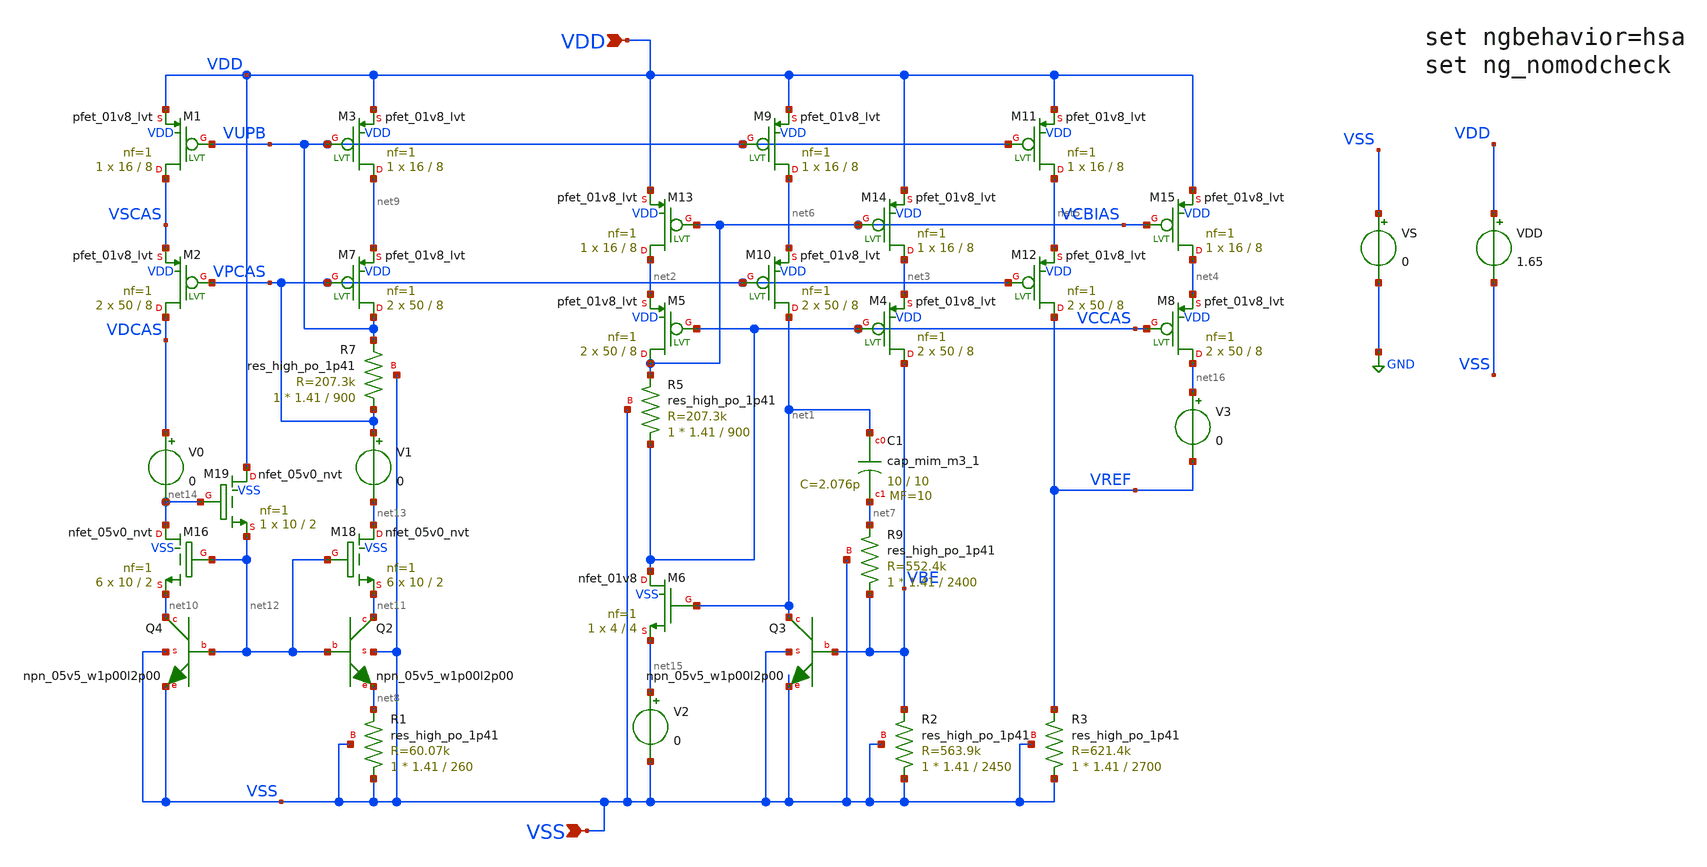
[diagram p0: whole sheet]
** sch_path: testbenches/parallel_bandgap_dc_sweep.sch
**.subckt parallel_bandgap_dc_sweep VDD VSS
*.ipin VDD
*.ipin VSS
VDD VDD VSS 1.65
.save i(vdd)
VS VSS GND 0
XQ3 net1 VBE VSS VSS sky130_fd_pr__npn_05v5_w1p00l2p00
XR2 VSS VBE VSS sky130_fd_pr__res_high_po_1p41 L=2450 mult=1 m=1
XM4 VBE VCCAS net3 VDD sky130_fd_pr__pfet_01v8_lvt L=8 W=50 nf=1 ad='int((nf+1)/2) * W/nf * 0.29' as='int((nf+2)/2) * W/nf * 0.29'
+ pd='2*int((nf+1)/2) * (W/nf + 0.29)' ps='2*int((nf+2)/2) * (W/nf + 0.29)' nrd='0.29 / W' nrs='0.29 / W'
+ sa=0 sb=0 sd=0 mult=2 m=2
XM5 VCBIAS VCCAS net2 VDD sky130_fd_pr__pfet_01v8_lvt L=8 W=50 nf=1 ad='int((nf+1)/2) * W/nf * 0.29'
+ as='int((nf+2)/2) * W/nf * 0.29' pd='2*int((nf+1)/2) * (W/nf + 0.29)' ps='2*int((nf+2)/2) * (W/nf + 0.29)'
+ nrd='0.29 / W' nrs='0.29 / W' sa=0 sb=0 sd=0 mult=2 m=2
XM6 VCCAS net1 net15 VSS sky130_fd_pr__nfet_01v8 L=4 W=4 nf=1 ad='int((nf+1)/2) * W/nf * 0.29' as='int((nf+2)/2) * W/nf * 0.29'
+ pd='2*int((nf+1)/2) * (W/nf + 0.29)' ps='2*int((nf+2)/2) * (W/nf + 0.29)' nrd='0.29 / W' nrs='0.29 / W'
+ sa=0 sb=0 sd=0 mult=1 m=1
XR3 VSS VREF VSS sky130_fd_pr__res_high_po_1p41 L=2700 mult=1 m=1
XM8 net16 VCCAS net4 VDD sky130_fd_pr__pfet_01v8_lvt L=8 W=50 nf=1 ad='int((nf+1)/2) * W/nf * 0.29' as='int((nf+2)/2) * W/nf * 0.29'
+ pd='2*int((nf+1)/2) * (W/nf + 0.29)' ps='2*int((nf+2)/2) * (W/nf + 0.29)' nrd='0.29 / W' nrs='0.29 / W'
+ sa=0 sb=0 sd=0 mult=2 m=2
XM9 net6 VUPB VDD VDD sky130_fd_pr__pfet_01v8_lvt L=8 W=16 nf=1 ad='int((nf+1)/2) * W/nf * 0.29' as='int((nf+2)/2) * W/nf * 0.29'
+ pd='2*int((nf+1)/2) * (W/nf + 0.29)' ps='2*int((nf+2)/2) * (W/nf + 0.29)' nrd='0.29 / W' nrs='0.29 / W'
+ sa=0 sb=0 sd=0 mult=1 m=1
XM10 net1 VPCAS net6 VDD sky130_fd_pr__pfet_01v8_lvt L=8 W=50 nf=1 ad='int((nf+1)/2) * W/nf * 0.29' as='int((nf+2)/2) * W/nf * 0.29'
+ pd='2*int((nf+1)/2) * (W/nf + 0.29)' ps='2*int((nf+2)/2) * (W/nf + 0.29)' nrd='0.29 / W' nrs='0.29 / W'
+ sa=0 sb=0 sd=0 mult=2 m=2
XM11 net5 VUPB VDD VDD sky130_fd_pr__pfet_01v8_lvt L=8 W=16 nf=1 ad='int((nf+1)/2) * W/nf * 0.29' as='int((nf+2)/2) * W/nf * 0.29'
+ pd='2*int((nf+1)/2) * (W/nf + 0.29)' ps='2*int((nf+2)/2) * (W/nf + 0.29)' nrd='0.29 / W' nrs='0.29 / W'
+ sa=0 sb=0 sd=0 mult=1 m=1
XM12 VREF VPCAS net5 VDD sky130_fd_pr__pfet_01v8_lvt L=8 W=50 nf=1 ad='int((nf+1)/2) * W/nf * 0.29' as='int((nf+2)/2) * W/nf * 0.29'
+ pd='2*int((nf+1)/2) * (W/nf + 0.29)' ps='2*int((nf+2)/2) * (W/nf + 0.29)' nrd='0.29 / W' nrs='0.29 / W'
+ sa=0 sb=0 sd=0 mult=2 m=2
XM13 net2 VCBIAS VDD VDD sky130_fd_pr__pfet_01v8_lvt L=8 W=16 nf=1 ad='int((nf+1)/2) * W/nf * 0.29' as='int((nf+2)/2) * W/nf * 0.29'
+ pd='2*int((nf+1)/2) * (W/nf + 0.29)' ps='2*int((nf+2)/2) * (W/nf + 0.29)' nrd='0.29 / W' nrs='0.29 / W'
+ sa=0 sb=0 sd=0 mult=1 m=1
XM14 net3 VCBIAS VDD VDD sky130_fd_pr__pfet_01v8_lvt L=8 W=16 nf=1 ad='int((nf+1)/2) * W/nf * 0.29' as='int((nf+2)/2) * W/nf * 0.29'
+ pd='2*int((nf+1)/2) * (W/nf + 0.29)' ps='2*int((nf+2)/2) * (W/nf + 0.29)' nrd='0.29 / W' nrs='0.29 / W'
+ sa=0 sb=0 sd=0 mult=1 m=1
XR5 VCCAS VCBIAS VSS sky130_fd_pr__res_high_po_1p41 L=900 mult=1 m=1
XM15 net4 VCBIAS VDD VDD sky130_fd_pr__pfet_01v8_lvt L=8 W=16 nf=1 ad='int((nf+1)/2) * W/nf * 0.29' as='int((nf+2)/2) * W/nf * 0.29'
+ pd='2*int((nf+1)/2) * (W/nf + 0.29)' ps='2*int((nf+2)/2) * (W/nf + 0.29)' nrd='0.29 / W' nrs='0.29 / W'
+ sa=0 sb=0 sd=0 mult=1 m=1
XR9 VBE net7 VSS sky130_fd_pr__res_high_po_1p41 L=2400 mult=1 m=1
XC1 net1 net7 sky130_fd_pr__cap_mim_m3_1 W=10 L=10 MF=10 m=10
V0 VDCAS net14 0
.save i(v0)
V1 VPCAS net13 0
.save i(v1)
XM3 net9 VUPB VDD VDD sky130_fd_pr__pfet_01v8_lvt L=8 W=16 nf=1 ad='int((nf+1)/2) * W/nf * 0.29' as='int((nf+2)/2) * W/nf * 0.29'
+ pd='2*int((nf+1)/2) * (W/nf + 0.29)' ps='2*int((nf+2)/2) * (W/nf + 0.29)' nrd='0.29 / W' nrs='0.29 / W'
+ sa=0 sb=0 sd=0 mult=1 m=1
XM1 VSCAS VUPB VDD VDD sky130_fd_pr__pfet_01v8_lvt L=8 W=16 nf=1 ad='int((nf+1)/2) * W/nf * 0.29' as='int((nf+2)/2) * W/nf * 0.29'
+ pd='2*int((nf+1)/2) * (W/nf + 0.29)' ps='2*int((nf+2)/2) * (W/nf + 0.29)' nrd='0.29 / W' nrs='0.29 / W'
+ sa=0 sb=0 sd=0 mult=1 m=1
XQ2 net11 net12 net8 VSS sky130_fd_pr__npn_05v5_w1p00l2p00
XQ4 net10 net12 VSS VSS sky130_fd_pr__npn_05v5_w1p00l2p00
XR1 VSS net8 VSS sky130_fd_pr__res_high_po_1p41 L=260 mult=1 m=1
XM7 VUPB VPCAS net9 VDD sky130_fd_pr__pfet_01v8_lvt L=8 W=50 nf=1 ad='int((nf+1)/2) * W/nf * 0.29' as='int((nf+2)/2) * W/nf * 0.29'
+ pd='2*int((nf+1)/2) * (W/nf + 0.29)' ps='2*int((nf+2)/2) * (W/nf + 0.29)' nrd='0.29 / W' nrs='0.29 / W'
+ sa=0 sb=0 sd=0 mult=2 m=2
XM2 VDCAS VPCAS VSCAS VDD sky130_fd_pr__pfet_01v8_lvt L=8 W=50 nf=1 ad='int((nf+1)/2) * W/nf * 0.29'
+ as='int((nf+2)/2) * W/nf * 0.29' pd='2*int((nf+1)/2) * (W/nf + 0.29)' ps='2*int((nf+2)/2) * (W/nf + 0.29)'
+ nrd='0.29 / W' nrs='0.29 / W' sa=0 sb=0 sd=0 mult=2 m=2
XR7 VPCAS VUPB VSS sky130_fd_pr__res_high_po_1p41 L=900 mult=1 m=1
XM16 net14 net12 net10 VSS sky130_fd_pr__nfet_05v0_nvt L=2 W=10 nf=1 ad='int((nf+1)/2) * W/nf * 0.29'
+ as='int((nf+2)/2) * W/nf * 0.29' pd='2*int((nf+1)/2) * (W/nf + 0.29)' ps='2*int((nf+2)/2) * (W/nf + 0.29)'
+ nrd='0.29 / W' nrs='0.29 / W' sa=0 sb=0 sd=0 mult=6 m=6
XM18 net13 net12 net11 VSS sky130_fd_pr__nfet_05v0_nvt L=2 W=10 nf=1 ad='int((nf+1)/2) * W/nf * 0.29'
+ as='int((nf+2)/2) * W/nf * 0.29' pd='2*int((nf+1)/2) * (W/nf + 0.29)' ps='2*int((nf+2)/2) * (W/nf + 0.29)'
+ nrd='0.29 / W' nrs='0.29 / W' sa=0 sb=0 sd=0 mult=6 m=6
XM19 VDD net14 net12 VSS sky130_fd_pr__nfet_05v0_nvt L=2 W=10 nf=1 ad='int((nf+1)/2) * W/nf * 0.29' as='int((nf+2)/2) * W/nf * 0.29'
+ pd='2*int((nf+1)/2) * (W/nf + 0.29)' ps='2*int((nf+2)/2) * (W/nf + 0.29)' nrd='0.29 / W' nrs='0.29 / W'
+ sa=0 sb=0 sd=0 mult=1 m=1
V2 net15 VSS 0
.save i(v2)
V3 net16 VREF 0
.save i(v3)
**** begin user architecture code


* ngspice commands
.option wnflag=1
.option savecurrents
.control
save all
dc temp -40 125 5
** remove zero length vectors to prevent write errors
remzerovec
write ~/.xschem/simulations/parallel_bandgap_dc_sweep.raw
wrdata ~/.xschem/simulations/parallel_bandgap_dc_sweep.txt V(VREF) I(V0)/I(V1) I(V2)/I(V3)
plot V(VREF)
plot I(V0)/I(V1)
set temp = 125
op
remzerovec
write ~/.xschem/simulations/parallel_bandgap_dc_sweep.raw
.endc



** opencircuitdesign pdks install
.lib /foss/pdks/sky130A/libs.tech/combined/sky130.corners.lib.spice fshl

**** end user architecture code
**.ends
.GLOBAL GND
.end
